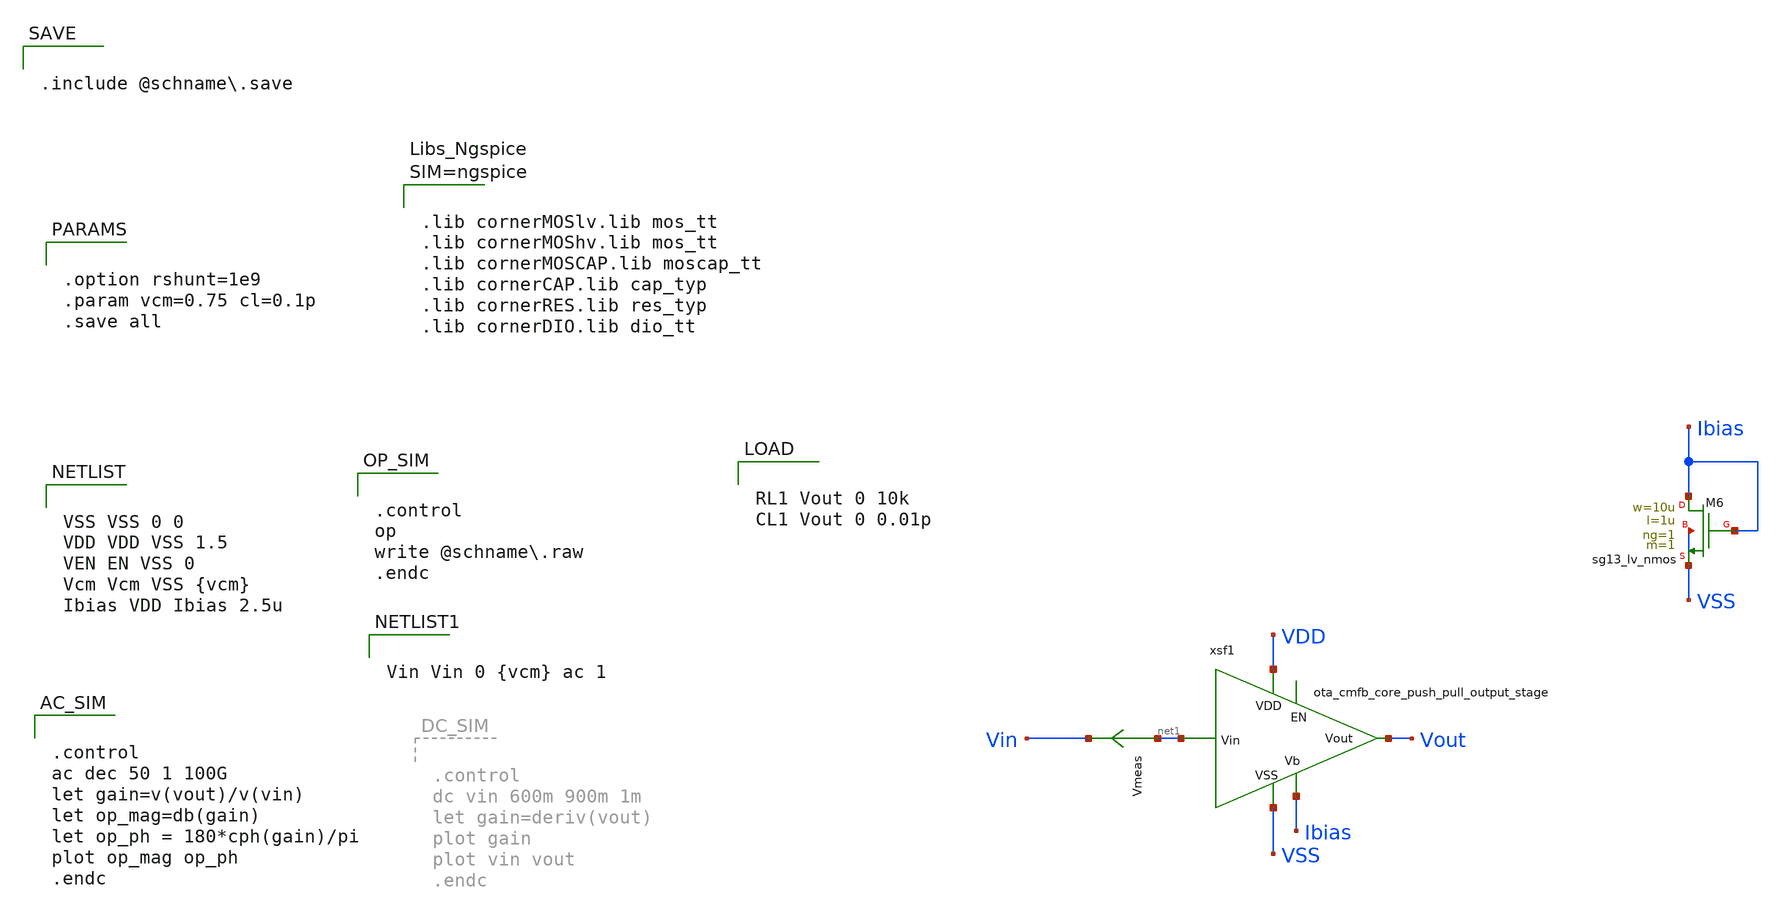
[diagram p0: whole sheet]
** sch_path: schema/ota_cmfb_core/ota_cmfb_core_push_pull_output_stage_tb.sch
**.subckt ota_cmfb_core_push_pull_output_stage_tb
XM6 Ibias Ibias VSS VSS sg13_lv_nmos w=10u l=1u ng=1 m=1 mm_ok=1
Vmeas net1 Vin 0
.save i(vmeas)
xsf1 VDD net1 Vout Ibias VSS ota_cmfb_core_push_pull_output_stage
**** begin user architecture code


VSS VSS 0 0
VDD VDD VSS 1.5
VEN EN VSS 0
Vcm Vcm VSS {vcm}
Ibias VDD Ibias 2.5u



.control
op
write @schname.raw
.endc



.control
ac dec 50 1 100G
let gain=v(vout)/v(vin)
let op_mag=db(gain)
let op_ph = 180*cph(gain)/pi
plot op_mag op_ph
.endc




.option rshunt=1e9
.param vcm=0.75 cl=0.1p
.save all




RL1 Vout 0 10k
CL1 Vout 0 0.01p



.include @schname.save



Vin Vin 0 {vcm} ac 1





.lib cornerMOSlv.lib mos_tt
.lib cornerMOShv.lib mos_tt
.lib cornerMOSCAP.lib moscap_tt
.lib cornerCAP.lib cap_typ
.lib cornerRES.lib res_typ
.lib cornerDIO.lib dio_tt



**** end user architecture code
**.ends

* expanding   symbol:  ota_cmfb_core/ota_cmfb_core_push_pull_output_stage.sym # of pins=5
** sym_path: schema/ota_cmfb_core/ota_cmfb_core_push_pull_output_stage.sym
** sch_path: schema/ota_cmfb_core/ota_cmfb_core_push_pull_output_stage.sch
.subckt ota_cmfb_core_push_pull_output_stage VDD Vin Vout Vbias VSS
*.iopin VSS
*.iopin VDD
*.ipin Vbias
*.ipin Vin
*.opin Vout
XM1 Vout Vin_shifted VSS VSS sg13_lv_nmos w=0.5u l=10u ng=1 m=1 mm_ok=1
XM2 VDD Vin Vout VDD sg13_lv_pmos w=5u l=0.5u ng=1 m=1 mm_ok=1
XMC VDD Vbiasp CD_DRN VDD sg13_lv_pmos w=2.5u l=3u ng=1 m=4 mm_ok=1
XME Vin_shifted Vcasp2 Vin VDD sg13_lv_pmos w=2.5u l=3u ng=1 m=2 mm_ok=1
XMD CD_DRN Vcasp Vin VDD sg13_lv_pmos w=2.5u l=3u ng=1 m=4 mm_ok=1
XMN Vin Vcasn2 Vin_shifted VSS sg13_lv_nmos w=0.7u l=3u ng=1 m=2 mm_ok=1
XMH VDD Vbiasp net1 VDD sg13_lv_pmos w=2.5u l=3u ng=1 m=4 mm_ok=1
XMI net1 Vcasp Vcasp VDD sg13_lv_pmos w=2.5u l=3u ng=1 m=4 mm_ok=1
XMJ Vcasp Vcasp2 Vcasp2 VDD sg13_lv_pmos w=2.5u l=3u ng=1 m=4 mm_ok=1
XMB VDD Vbiasp Vcasn2 VDD sg13_lv_pmos w=2.5u l=3u ng=1 m=4 mm_ok=1
XMO Vcasn2 Vcasn2 Vcasn VSS sg13_lv_nmos w=0.7u l=3u ng=1 m=4 mm_ok=1
XR1 net2 Vout VSS rhigh w=0.5e-6 l=1e-6*8 m=1 b=0 mm_ok=1
XC1 Vin net2 sg13_moscap_p w=3.5u l=21.5u m=1 mm_ok=1
XMFG Vbiasp Vbias VSS VSS sg13_lv_nmos w=0.25u l=10u ng=1 m=2 mm_ok=1
XMA VDD Vbiasp Vbiasp VDD sg13_lv_pmos w=2.5u l=3u ng=1 m=10 mm_ok=1
XMP Vcasn Vcasn Vbiasn VSS sg13_lv_nmos w=0.7u l=3u ng=1 m=4 mm_ok=1
XMQ Vbiasn Vbiasn VSS VSS sg13_lv_nmos w=0.7u l=3u ng=1 m=4 mm_ok=1
XMM Vin_shifted Vcasn src_ml VSS sg13_lv_nmos w=0.7u l=3u ng=1 m=4 mm_ok=1
XML src_ml Vbiasn VSS VSS sg13_lv_nmos w=0.7u l=3u ng=1 m=4 mm_ok=1
XMK Vcasp2 Vbiasn VSS VSS sg13_lv_nmos w=0.7u l=3u ng=1 m=4 mm_ok=1
XM3 CD_DRN VDD VDD VDD sg13_lv_pmos w=2.5u l=0.5u ng=1 m=2 mm_ok=1
XM4 Vin_shifted VDD VDD VDD sg13_lv_pmos w=2.5u l=0.5u ng=1 m=1 mm_ok=1
XM5 Vbiasp VDD VDD VDD sg13_lv_pmos w=2.5u l=0.5u ng=1 m=1 mm_ok=1
XM6 Vin VDD VDD VDD sg13_lv_pmos w=2.5u l=0.5u ng=1 m=1 mm_ok=1
XM7 VSS VSS Vin_shifted VSS sg13_lv_nmos w=0.7u l=0.5u ng=1 m=2 mm_ok=1
XM8 VSS VSS Vcasn VSS sg13_lv_nmos w=0.7u l=0.5u ng=1 m=4 mm_ok=1
XMX VSS VSS Vin_shifted VSS sg13_lv_nmos w=0.7u l=3u ng=1 m=4 mm_ok=1
XM9 VSS VSS src_ml VSS sg13_lv_nmos w=0.7u l=0.5u ng=1 m=4 mm_ok=1
XM10 Vcasp VDD VDD VDD sg13_lv_pmos w=2.5u l=0.5u ng=1 m=2 mm_ok=1
XM12 VSS VSS Vbiasp VSS sg13_lv_nmos w=0.25u l=0.5u ng=1 m=2 mm_ok=1
.ends

.end
